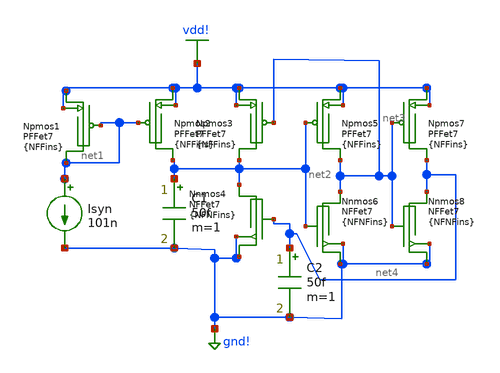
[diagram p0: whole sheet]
** sch_path: SimulationModeling/BesrourStatic.sch
**.subckt BesrourStatic
Npmos2 vdd! net1 net2 vdd! BSIMCMG_osdi_P nfin={NFFins}
Npmos5 vdd! net2 net3 vdd! BSIMCMG_osdi_P nfin={NFFins}
Npmos7 vdd! net3 net4 vdd! BSIMCMG_osdi_P nfin={NFFins}
Nnmos6 gnd! net2 net3 gnd! BSIMCMG_osdi_N nfin={NFNFins}
Nnmos8 gnd! net3 net4 gnd! BSIMCMG_osdi_N nfin={NFNFins}
C2 net4 gnd! 50f m=1
C1 net2 gnd! 50f m=1
Npmos1 vdd! net1 net1 vdd! BSIMCMG_osdi_P nfin={NFFins}
Npmos3 vdd! net3 net2 vdd! BSIMCMG_osdi_P nfin={NFFins}
Nnmos4 gnd! net4 net2 gnd! BSIMCMG_osdi_N nfin={NFNFins}
Isyn net1 gnd! 101n
**** begin user architecture code



* ngspice commands
.include asap7_TT_slvt.sp
.param NFFins=1
.param NFNFins=5
Vvdd vdd! 0 dc=0.7
Vgnd gnd! 0 dc=0
.ic v(net2)=0 v(net4)=0
.control
    set maxstep = 0.01n

    set method = gear
    set gmin = 1e-15

    set itl1 = 1000
    set itl4 = 1000
    set num_threads = 24
    set parallel = 1
    set filetype=ascii
    set wr_vecnames
    set wr_singlescale

    echo VDD Static_Power > /Users/logan/Desktop/besrourneuron.txt

    alter Isyn = 0

    alter C1 = 1e-15
    alter C2 = 1e-15

    foreach vdd 0.1 0.11 0.12 0.13 0.14 0.15 0.16 0.17 0.18 0.19 0.2 0.21 0.22 0.23 0.24 0.25 0.26
+ 0.27 0.28 0.29 0.3 0.31 0.32 0.33 0.34 0.35 0.36 0.37 0.38 0.39 0.4 0.41 0.42 0.43 0.44 0.45 0.46 0.47
+ 0.48 0.49 0.5 0.51 0.52 0.53 0.54 0.55 0.56 0.57 0.58 0.59 0.6 0.61 0.62 0.63 0.64 0.65 0.66 0.67 0.68
+ 0.69 0.7 0.71 0.72 0.73 0.74 0.75 0.76 0.77 0.78 0.79 0.8 0.81 0.82 0.83 0.84 0.85 0.86 0.87 0.88 0.89
+ 0.9
        alter Vvdd dc=$vdd

        tran 0.04n 20n UIC

        let power_vdd = -1*v(vdd!)*i(Vvdd)
        let n_points = length(power_vdd)
        let start_idx = n_points - floor(n_points/5)

        * Calculate average power over last 20% of simulation points
        let i = $&start_idx
        let sum_power = 0

        dowhile i < n_points
            let sum_power = sum_power + power_vdd[i]
            let i = i + 1
        end

        let static_power = sum_power / (n_points - $&start_idx)

        echo $vdd $&static_power >> /Users/logan/Desktop/besrourneuron.txt
        echo At VDD=$vdd V Static_Power=$&static_power W
    end
.endc



**** end user architecture code
**.ends
.GLOBAL vdd!
.GLOBAL gnd!
.end
